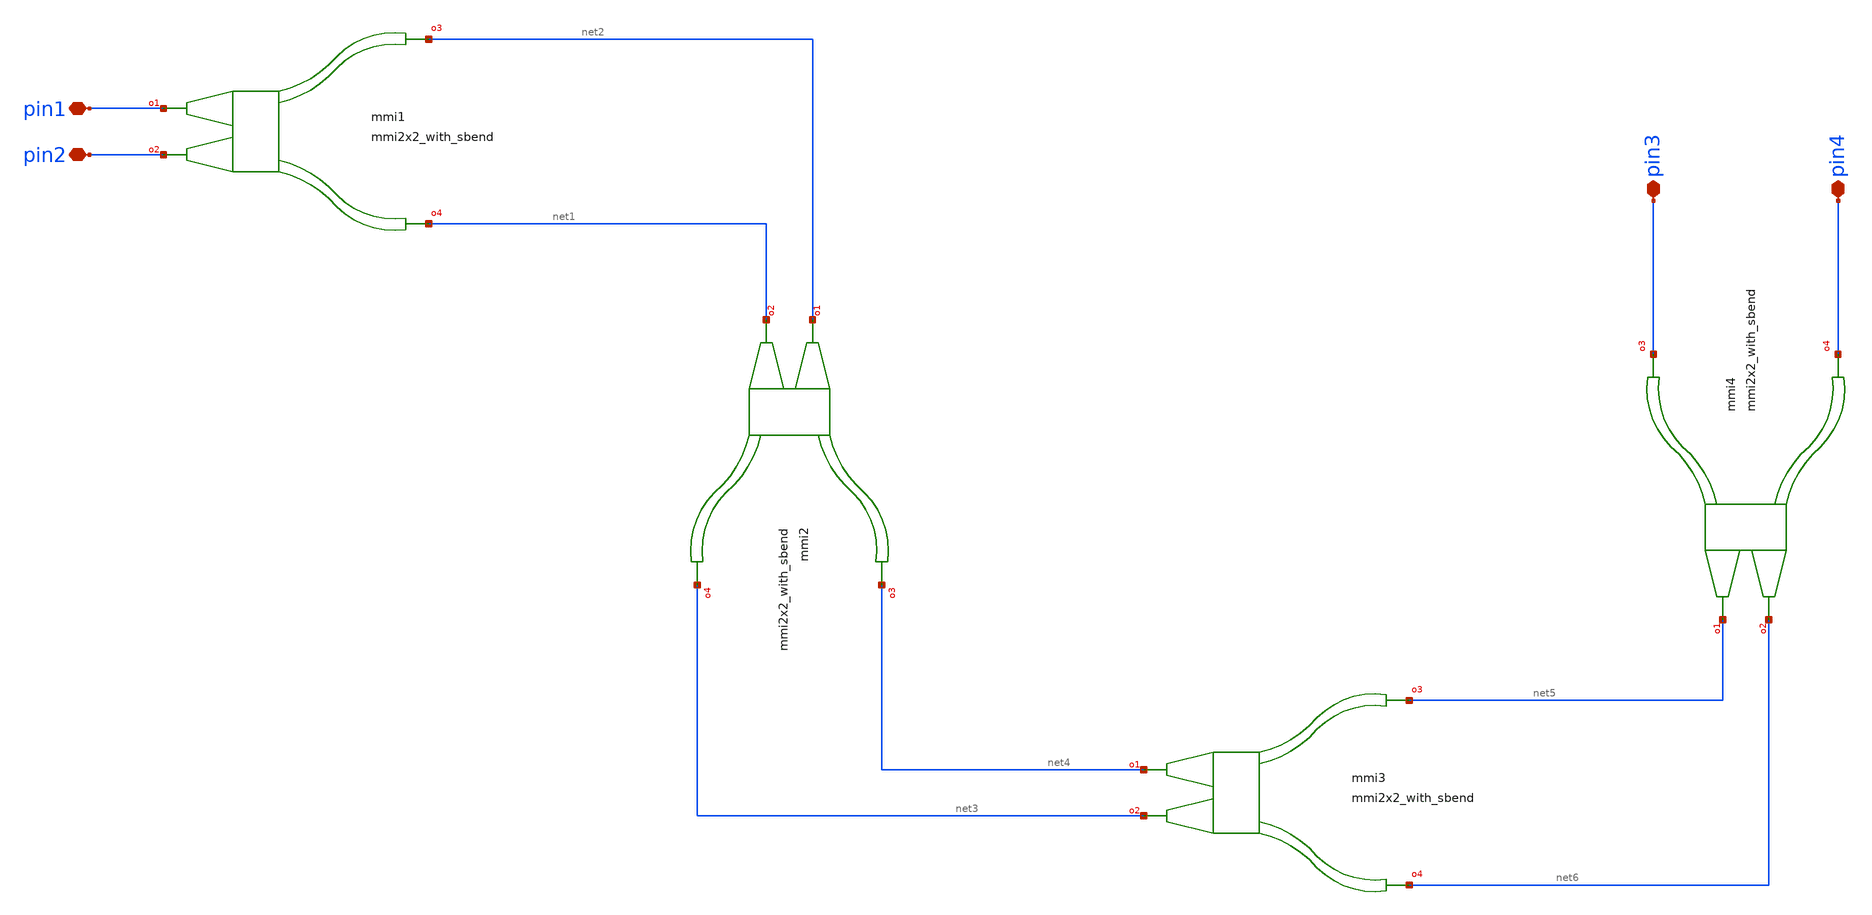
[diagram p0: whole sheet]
** sch_path: xschem/tests/test_sch/test_mmi2x2_with_sbend.sch
* Copyright (c) 2024, Mabrains LLC
* Licensed under the GNU Lesser General Public License, Version 3.0 (the "License");
* you may not use this file except in compliance with the License.
* GNU Lesser General Public License
* Version 3, 29 June 2007
* This program is free software: you can redistribute it and/or modify
* it under the terms of the GNU Lesser General Public License as published
* by the Free Software Foundation, either version 3 of the License, or
* (at your option) any later version.
* This program is distributed in the hope that it will be useful,
* but WITHOUT ANY WARRANTY; without even the implied warranty of
* MERCHANTABILITY or FITNESS FOR A PARTICULAR PURPOSE.  See the
* GNU Lesser General Public License for more details.
* You should have received a copy of the GNU Lesser General Public License
* along with this program.  If not, see <https://www.gnu.org/licenses/>.
* SPDX-License-Identifier: LGPL-3.0
**.subckt test_mmi2x2_with_sbend pin1 pin2 pin3 pin4
*.iopin pin1
*.iopin pin2
*.iopin pin3
*.iopin pin4
Pmmi1 pin1 pin2 net2 net1 mmi2x2_with_sbend
Pmmi2 net2 net1 net4 net3 mmi2x2_with_sbend
Pmmi3 net4 net3 net5 net6 mmi2x2_with_sbend
Pmmi4 net5 net6 pin3 pin4 mmi2x2_with_sbend
**.ends
.end
